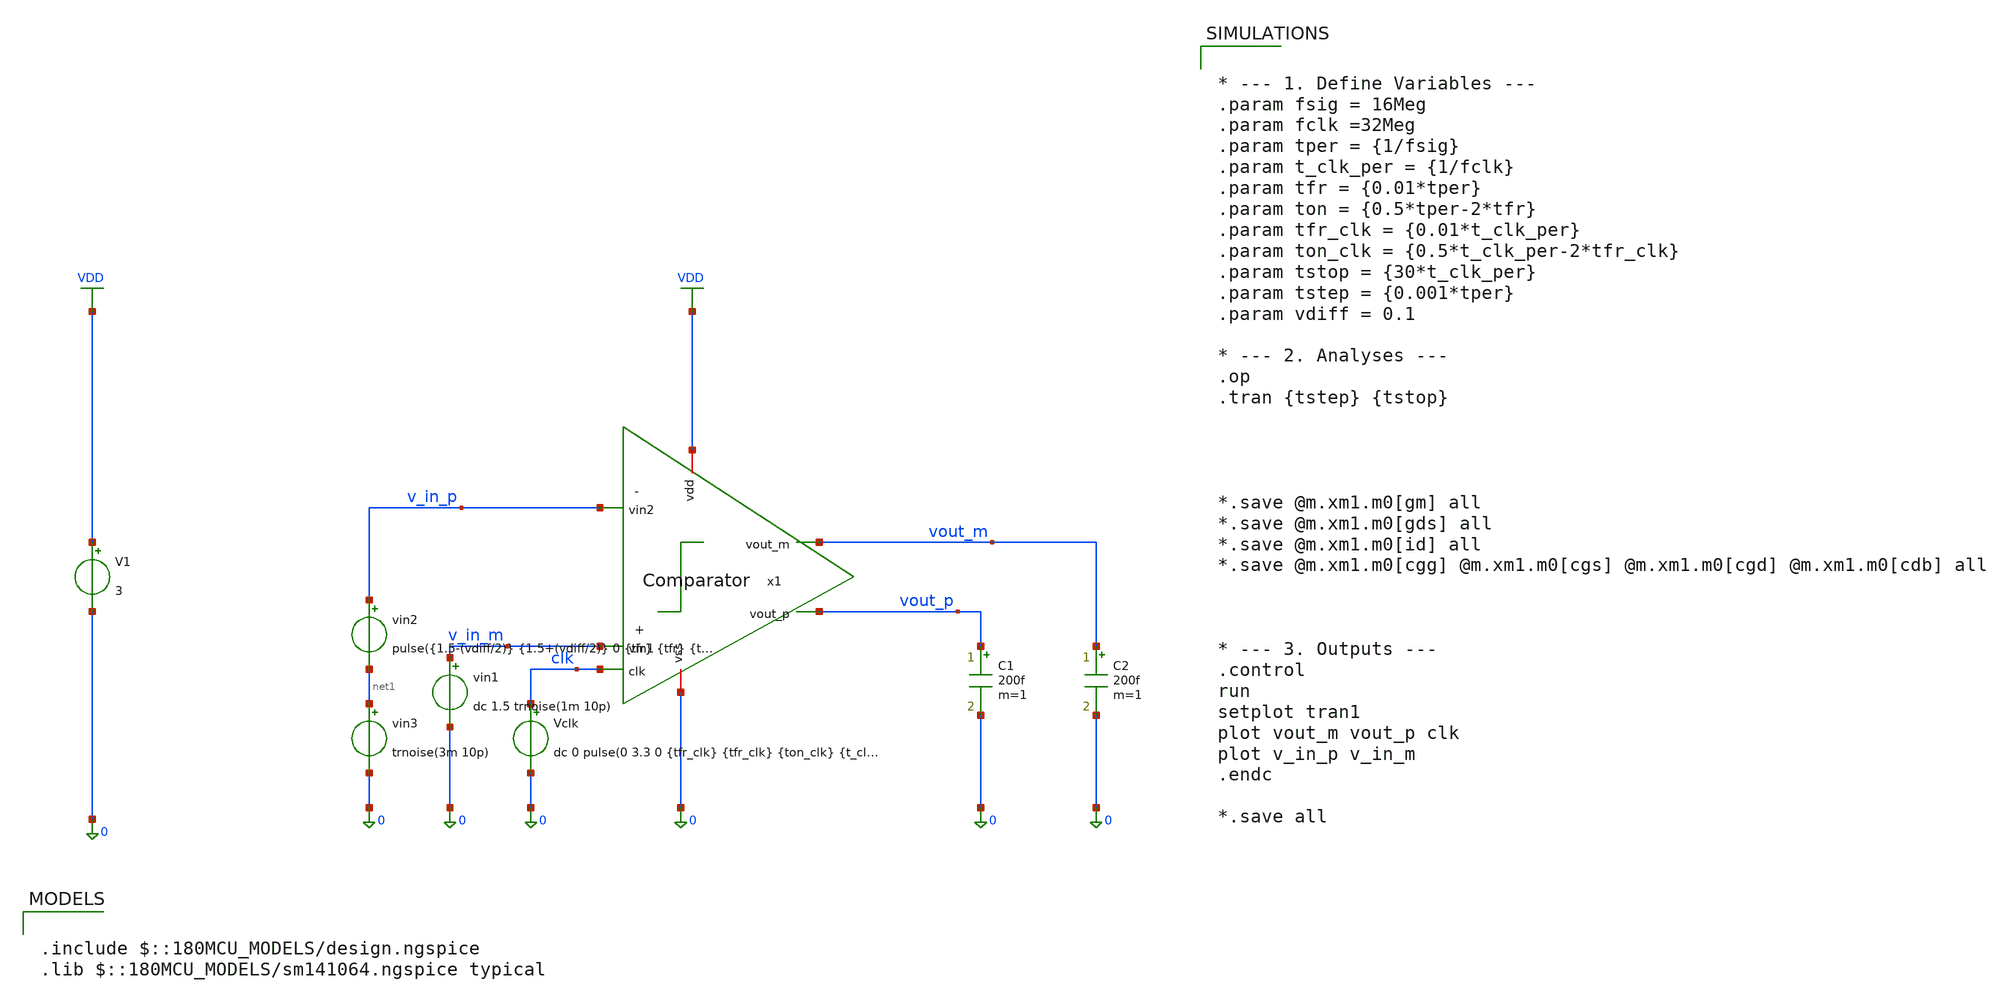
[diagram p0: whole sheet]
** sch_path: General/ADC/Comparator/Comparator_tb.sch
**.subckt Comparator_tb
x1 VDD vout_m vout_p v_in_p v_in_m clk 0 Comparator
V1 VDD 0 3
vin2 v_in_p net1 pulse({1.5-(vdiff/2)} {1.5+(vdiff/2)} 0 {tfr} {tfr} {ton} {tper})
vin1 v_in_m 0 dc 1.5 trnoise(1m 10p)
Vclk clk 0 dc 0 pulse(0 3.3 0 {tfr_clk} {tfr_clk} {ton_clk} {t_clk_per})
C1 vout_p 0 200f m=1
C2 vout_m 0 200f m=1
vin3 net1 0 trnoise(3m 10p)
**** begin user architecture code


* --- 1. Define Variables ---
.param fsig = 16Meg
.param fclk =32Meg
.param tper = {1/fsig}
.param t_clk_per = {1/fclk}
.param tfr = {0.01*tper}
.param ton = {0.5*tper-2*tfr}
.param tfr_clk = {0.01*t_clk_per}
.param ton_clk = {0.5*t_clk_per-2*tfr_clk}
.param tstop = {30*t_clk_per}
.param tstep = {0.001*tper}
.param vdiff = 0.1

* --- 2. Analyses ---
.op
.tran {tstep} {tstop}




*.save @m.xm1.m0[gm] all
*.save @m.xm1.m0[gds] all
*.save @m.xm1.m0[id] all
*.save @m.xm1.m0[cgg] @m.xm1.m0[cgs] @m.xm1.m0[cgd] @m.xm1.m0[cdb] all



* --- 3. Outputs ---
.control
run
setplot tran1
plot vout_m vout_p clk
plot v_in_p v_in_m
.endc

*.save all



.include $::180MCU_MODELS/design.ngspice
.lib $::180MCU_MODELS/sm141064.ngspice typical

**** end user architecture code
**.ends
.GLOBAL VDD
.end
